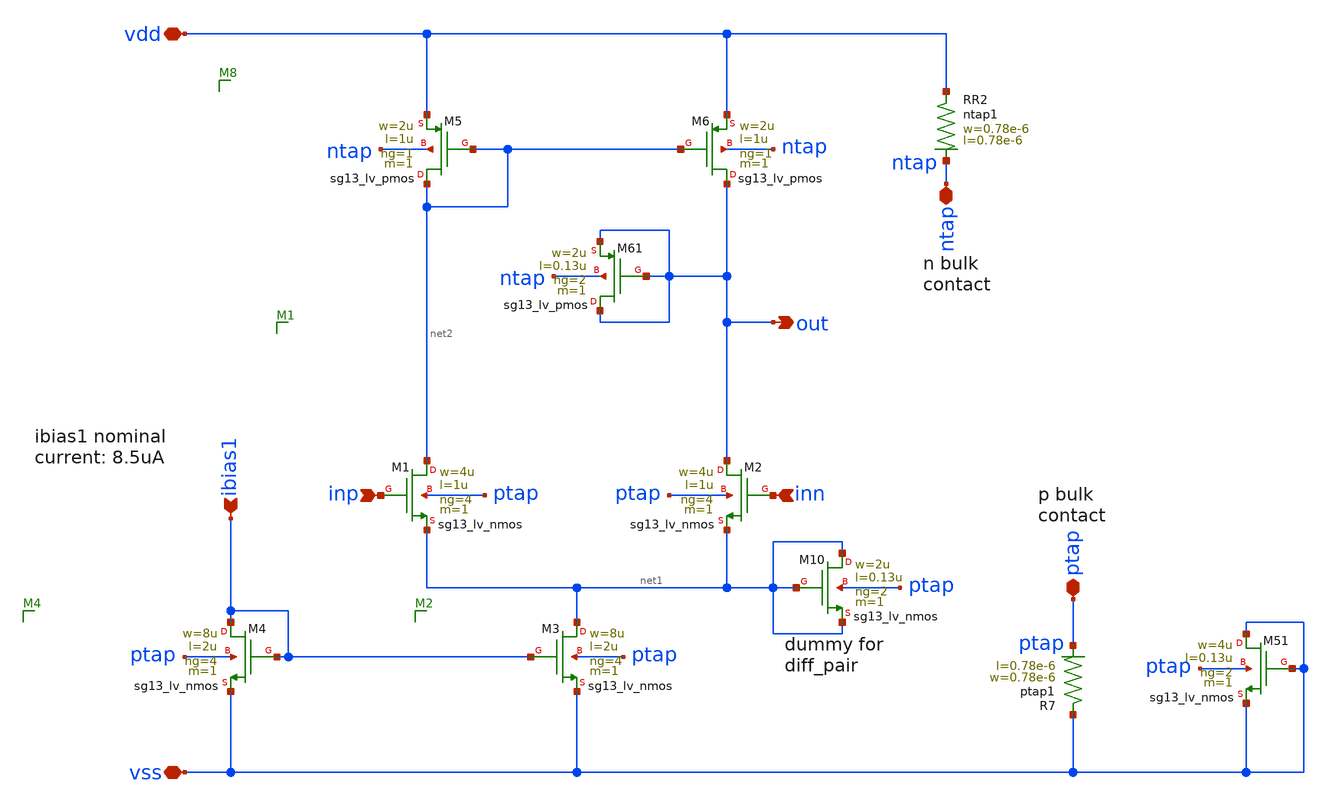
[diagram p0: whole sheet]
** sch_path: examples/ota/sch/ota.sch
**.subckt ota inn vdd vss inp ibias1 ntap ptap out
*.ipin inn
*.iopin vdd
*.iopin vss
*.ipin inp
*.ipin ibias1
*.iopin ntap
*.iopin ptap
*.opin out
XM1 net2 inp net1 ptap sg13_lv_nmos w=4u l=1u ng=4 m=1 mm_ok=1
XM2 out inn net1 ptap sg13_lv_nmos w=4u l=1u ng=4 m=1 mm_ok=1
XM3 net1 ibias1 vss ptap sg13_lv_nmos w=8u l=2u ng=4 m=1 mm_ok=1
XM4 ibias1 ibias1 vss ptap sg13_lv_nmos w=8u l=2u ng=4 m=1 mm_ok=1
XM5 net2 net2 vdd ntap sg13_lv_pmos w=2u l=1u ng=1 m=1 mm_ok=1
XM6 out net2 vdd ntap sg13_lv_pmos w=2u l=1u ng=1 m=1 mm_ok=1
XR2 vdd ntap ntap1 R=262.8 w=0.78e-6 l=0.78e-6
XM10 net1 net1 net1 ptap sg13_lv_nmos w=2u l=0.13u ng=2 m=1 mm_ok=1
XR7 vss ptap ptap1 R=262.8 w=0.78e-6 l=0.78e-6
XM51 vss vss vss ptap sg13_lv_nmos w=4u l=0.13u ng=2 m=1 mm_ok=1
XM61 out out out ntap sg13_lv_pmos w=2u l=0.13u ng=2 m=1 mm_ok=1
**.ends
.end
